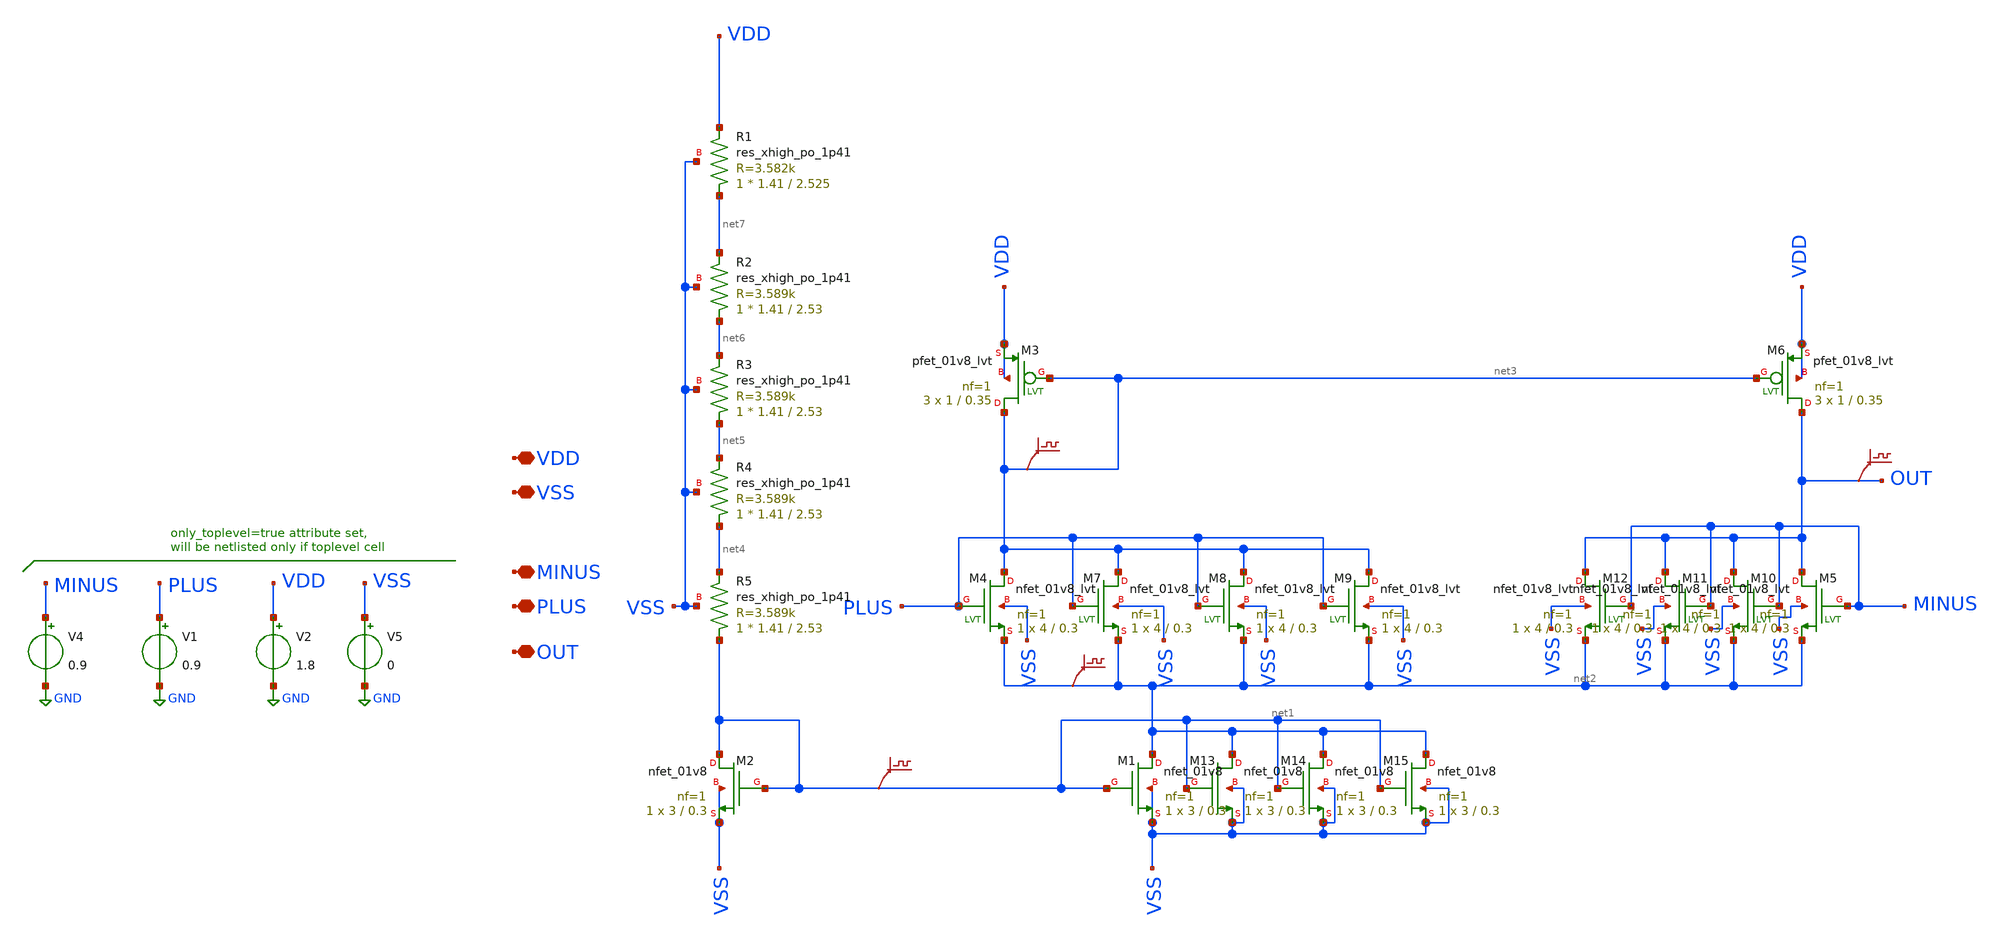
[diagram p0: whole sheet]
** sch_path: five_T_OTA.sch
**.subckt five_T_OTA VDD VSS MINUS PLUS OUT
*.iopin VDD
*.iopin VSS
*.iopin MINUS
*.iopin PLUS
*.iopin OUT
XM2 net1 net1 VSS VSS sky130_fd_pr__nfet_01v8 L=0.3 W=3 nf=1 ad='int((nf+1)/2) * W/nf * 0.29' as='int((nf+2)/2) * W/nf * 0.29'
+ pd='2*int((nf+1)/2) * (W/nf + 0.29)' ps='2*int((nf+2)/2) * (W/nf + 0.29)' nrd='0.29 / W' nrs='0.29 / W'
+ sa=0 sb=0 sd=0 mult=1 m=1
XM1 net2 net1 VSS VSS sky130_fd_pr__nfet_01v8 L=0.3 W=3 nf=1 ad='int((nf+1)/2) * W/nf * 0.29' as='int((nf+2)/2) * W/nf * 0.29'
+ pd='2*int((nf+1)/2) * (W/nf + 0.29)' ps='2*int((nf+2)/2) * (W/nf + 0.29)' nrd='0.29 / W' nrs='0.29 / W'
+ sa=0 sb=0 sd=0 mult=1 m=1
.save v(net1)
.save v(out)
.save v(net3)
.save v(net2)
XM4 net3 PLUS net2 VSS sky130_fd_pr__nfet_01v8_lvt L=0.3 W=4 nf=1 ad='int((nf+1)/2) * W/nf * 0.29' as='int((nf+2)/2) * W/nf * 0.29'
+ pd='2*int((nf+1)/2) * (W/nf + 0.29)' ps='2*int((nf+2)/2) * (W/nf + 0.29)' nrd='0.29 / W' nrs='0.29 / W'
+ sa=0 sb=0 sd=0 mult=1 m=1
XM5 OUT MINUS net2 VSS sky130_fd_pr__nfet_01v8_lvt L=0.3 W=4 nf=1 ad='int((nf+1)/2) * W/nf * 0.29' as='int((nf+2)/2) * W/nf * 0.29'
+ pd='2*int((nf+1)/2) * (W/nf + 0.29)' ps='2*int((nf+2)/2) * (W/nf + 0.29)' nrd='0.29 / W' nrs='0.29 / W'
+ sa=0 sb=0 sd=0 mult=1 m=1
XM3 net3 net3 VDD VDD sky130_fd_pr__pfet_01v8_lvt L=0.35 W=1 nf=1 ad='int((nf+1)/2) * W/nf * 0.29' as='int((nf+2)/2) * W/nf * 0.29'
+ pd='2*int((nf+1)/2) * (W/nf + 0.29)' ps='2*int((nf+2)/2) * (W/nf + 0.29)' nrd='0.29 / W' nrs='0.29 / W'
+ sa=0 sb=0 sd=0 mult=3 m=3
XM6 OUT net3 VDD VDD sky130_fd_pr__pfet_01v8_lvt L=0.35 W=1 nf=1 ad='int((nf+1)/2) * W/nf * 0.29' as='int((nf+2)/2) * W/nf * 0.29'
+ pd='2*int((nf+1)/2) * (W/nf + 0.29)' ps='2*int((nf+2)/2) * (W/nf + 0.29)' nrd='0.29 / W' nrs='0.29 / W'
+ sa=0 sb=0 sd=0 mult=3 m=3
XR5 net1 net4 VSS sky130_fd_pr__res_xhigh_po_1p41 L=2.53 mult=1 m=1
XM7 net3 PLUS net2 VSS sky130_fd_pr__nfet_01v8_lvt L=0.3 W=4 nf=1 ad='int((nf+1)/2) * W/nf * 0.29' as='int((nf+2)/2) * W/nf * 0.29'
+ pd='2*int((nf+1)/2) * (W/nf + 0.29)' ps='2*int((nf+2)/2) * (W/nf + 0.29)' nrd='0.29 / W' nrs='0.29 / W'
+ sa=0 sb=0 sd=0 mult=1 m=1
XM8 net3 PLUS net2 VSS sky130_fd_pr__nfet_01v8_lvt L=0.3 W=4 nf=1 ad='int((nf+1)/2) * W/nf * 0.29' as='int((nf+2)/2) * W/nf * 0.29'
+ pd='2*int((nf+1)/2) * (W/nf + 0.29)' ps='2*int((nf+2)/2) * (W/nf + 0.29)' nrd='0.29 / W' nrs='0.29 / W'
+ sa=0 sb=0 sd=0 mult=1 m=1
XM9 net3 PLUS net2 VSS sky130_fd_pr__nfet_01v8_lvt L=0.3 W=4 nf=1 ad='int((nf+1)/2) * W/nf * 0.29' as='int((nf+2)/2) * W/nf * 0.29'
+ pd='2*int((nf+1)/2) * (W/nf + 0.29)' ps='2*int((nf+2)/2) * (W/nf + 0.29)' nrd='0.29 / W' nrs='0.29 / W'
+ sa=0 sb=0 sd=0 mult=1 m=1
XM10 OUT MINUS net2 VSS sky130_fd_pr__nfet_01v8_lvt L=0.3 W=4 nf=1 ad='int((nf+1)/2) * W/nf * 0.29' as='int((nf+2)/2) * W/nf * 0.29'
+ pd='2*int((nf+1)/2) * (W/nf + 0.29)' ps='2*int((nf+2)/2) * (W/nf + 0.29)' nrd='0.29 / W' nrs='0.29 / W'
+ sa=0 sb=0 sd=0 mult=1 m=1
XM11 OUT MINUS net2 VSS sky130_fd_pr__nfet_01v8_lvt L=0.3 W=4 nf=1 ad='int((nf+1)/2) * W/nf * 0.29' as='int((nf+2)/2) * W/nf * 0.29'
+ pd='2*int((nf+1)/2) * (W/nf + 0.29)' ps='2*int((nf+2)/2) * (W/nf + 0.29)' nrd='0.29 / W' nrs='0.29 / W'
+ sa=0 sb=0 sd=0 mult=1 m=1
XM12 OUT MINUS net2 VSS sky130_fd_pr__nfet_01v8_lvt L=0.3 W=4 nf=1 ad='int((nf+1)/2) * W/nf * 0.29' as='int((nf+2)/2) * W/nf * 0.29'
+ pd='2*int((nf+1)/2) * (W/nf + 0.29)' ps='2*int((nf+2)/2) * (W/nf + 0.29)' nrd='0.29 / W' nrs='0.29 / W'
+ sa=0 sb=0 sd=0 mult=1 m=1
XM13 net2 net1 VSS VSS sky130_fd_pr__nfet_01v8 L=0.3 W=3 nf=1 ad='int((nf+1)/2) * W/nf * 0.29' as='int((nf+2)/2) * W/nf * 0.29'
+ pd='2*int((nf+1)/2) * (W/nf + 0.29)' ps='2*int((nf+2)/2) * (W/nf + 0.29)' nrd='0.29 / W' nrs='0.29 / W'
+ sa=0 sb=0 sd=0 mult=1 m=1
XM14 net2 net1 VSS VSS sky130_fd_pr__nfet_01v8 L=0.3 W=3 nf=1 ad='int((nf+1)/2) * W/nf * 0.29' as='int((nf+2)/2) * W/nf * 0.29'
+ pd='2*int((nf+1)/2) * (W/nf + 0.29)' ps='2*int((nf+2)/2) * (W/nf + 0.29)' nrd='0.29 / W' nrs='0.29 / W'
+ sa=0 sb=0 sd=0 mult=1 m=1
XM15 net2 net1 VSS VSS sky130_fd_pr__nfet_01v8 L=0.3 W=3 nf=1 ad='int((nf+1)/2) * W/nf * 0.29' as='int((nf+2)/2) * W/nf * 0.29'
+ pd='2*int((nf+1)/2) * (W/nf + 0.29)' ps='2*int((nf+2)/2) * (W/nf + 0.29)' nrd='0.29 / W' nrs='0.29 / W'
+ sa=0 sb=0 sd=0 mult=1 m=1
XR4 net4 net5 VSS sky130_fd_pr__res_xhigh_po_1p41 L=2.53 mult=1 m=1
XR3 net5 net6 VSS sky130_fd_pr__res_xhigh_po_1p41 L=2.53 mult=1 m=1
XR2 net6 net7 VSS sky130_fd_pr__res_xhigh_po_1p41 L=2.53 mult=1 m=1
XR1 net7 VDD VSS sky130_fd_pr__res_xhigh_po_1p41 L=2.525 mult=1 m=1
V1 PLUS GND 0.9
V4 MINUS GND 0.9
V5 VSS GND 0
V2 VDD GND 1.8
**** begin user architecture code

** opencircuitdesign pdks install
.lib $::SKYWATER_MODELS/sky130.lib.spice tt




.control

save @m.xm1.msky130_fd_pr__nfet_01v8[gm]
save @m.xm1.msky130_fd_pr__nfet_01v8[vth]
save @m.xm1.msky130_fd_pr__nfet_01v8[vdsat]
save @m.xm1.msky130_fd_pr__nfet_01v8[vds]
save @m.xm1.msky130_fd_pr__nfet_01v8[id]
save @m.xm1.msky130_fd_pr__nfet_01v8[gds]

save @m.xm2.msky130_fd_pr__nfet_01v8[gm]
save @m.xm2.msky130_fd_pr__nfet_01v8[vth]
save @m.xm2.msky130_fd_pr__nfet_01v8[vdsat]
save @m.xm2.msky130_fd_pr__nfet_01v8[vds]
save @m.xm2.msky130_fd_pr__nfet_01v8[id]
save @m.xm2.msky130_fd_pr__nfet_01v8[gds]

save @m.xm5.msky130_fd_pr__nfet_01v8_lvt[gm]
save @m.xm5.msky130_fd_pr__nfet_01v8_lvt[vth]
save @m.xm5.msky130_fd_pr__nfet_01v8_lvt[vdsat]
save @m.xm5.msky130_fd_pr__nfet_01v8_lvt[vds]
save @m.xm5.msky130_fd_pr__nfet_01v8_lvt[id]
save @m.xm5.msky130_fd_pr__nfet_01v8_lvt[gds]

save @m.xm6.msky130_fd_pr__pfet_01v8_lvt[gm]
save @m.xm6.msky130_fd_pr__pfet_01v8_lvt[vth]
save @m.xm6.msky130_fd_pr__pfet_01v8_lvt[vdsat]
save @m.xm6.msky130_fd_pr__pfet_01v8_lvt[vds]
save @m.xm6.msky130_fd_pr__pfet_01v8_lvt[id]
save @m.xm6.msky130_fd_pr__pfet_01v8_lvt[gds]


save all

op
write five_T_OTA.raw

.endc


**** end user architecture code
**.ends
.GLOBAL GND
.end
